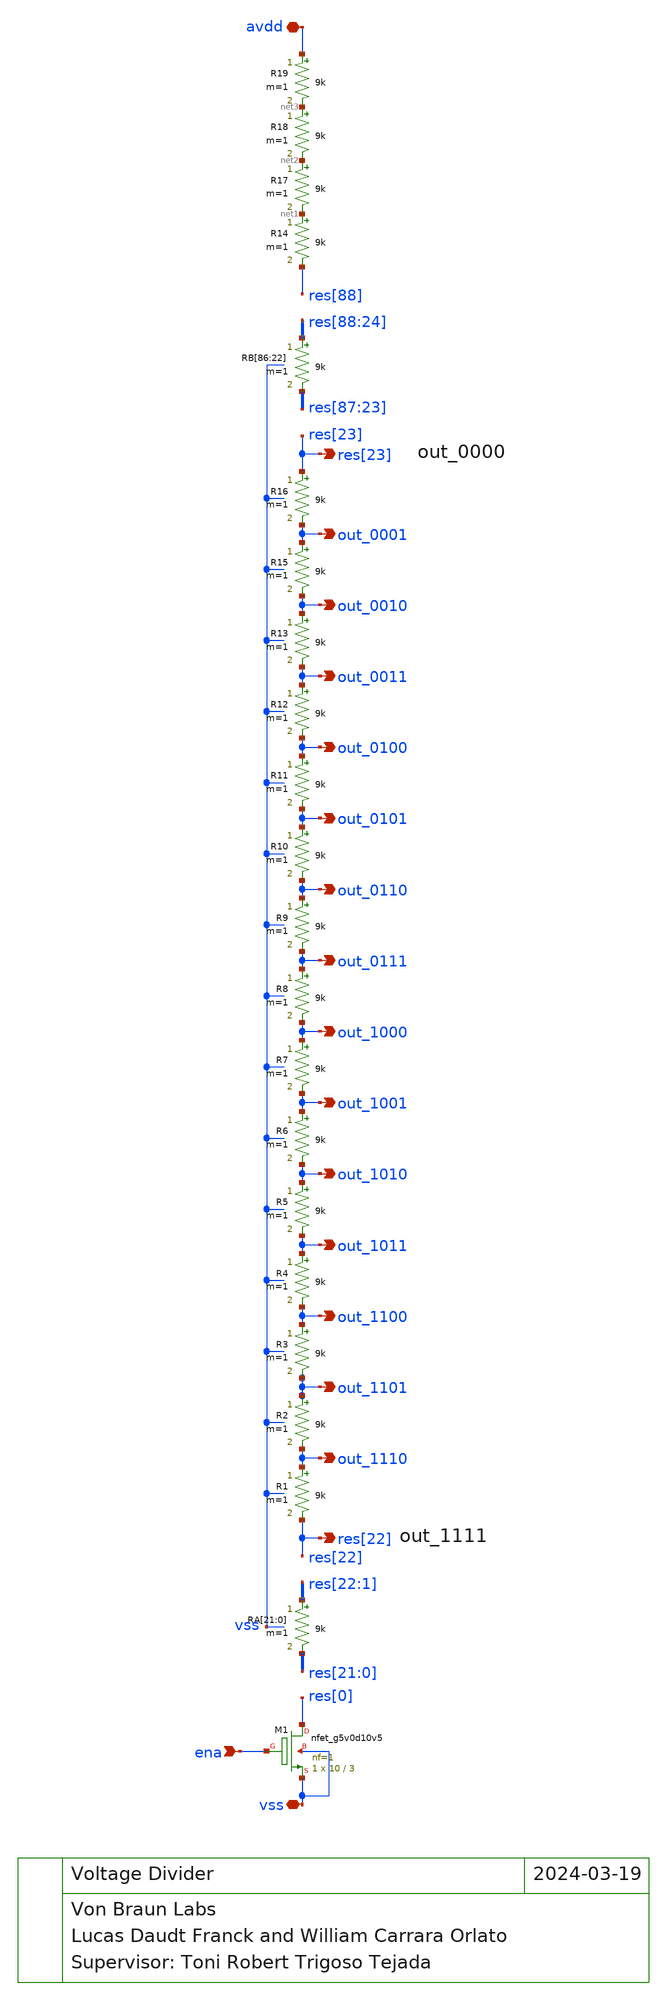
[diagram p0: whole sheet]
** sch_path: blocks/input/xschem/divisor_completo.sch
**.subckt divisor_completo ena vss avdd res[22] out_1110 out_1101 out_1100 out_1011 out_1010
*+ out_1001 out_1000 out_0111 out_0110 out_0101 out_0100 out_0011 out_0010 out_0001 res[23]
*.ipin ena
*.iopin vss
*.iopin avdd
*.opin res[22]
*.opin out_1110
*.opin out_1101
*.opin out_1100
*.opin out_1011
*.opin out_1010
*.opin out_1001
*.opin out_1000
*.opin out_0111
*.opin out_0110
*.opin out_0101
*.opin out_0100
*.opin out_0011
*.opin out_0010
*.opin out_0001
*.opin res[23]
XM1 res[0] ena vss vss sky130_fd_pr__nfet_g5v0d10v5 L=3 W=10 nf=1 ad='int((nf+1)/2) * W/nf * 0.29' as='int((nf+2)/2) * W/nf * 0.29'
+ pd='2*int((nf+1)/2) * (W/nf + 0.29)' ps='2*int((nf+2)/2) * (W/nf + 0.29)' nrd='0.29 / W' nrs='0.29 / W'
+ sa=0 sb=0 sd=0 mult=1 m=1
RA[21] res[22] res[21] 9k m=1
RA[20] res[21] res[20] 9k m=1
RA[19] res[20] res[19] 9k m=1
RA[18] res[19] res[18] 9k m=1
RA[17] res[18] res[17] 9k m=1
RA[16] res[17] res[16] 9k m=1
RA[15] res[16] res[15] 9k m=1
RA[14] res[15] res[14] 9k m=1
RA[13] res[14] res[13] 9k m=1
RA[12] res[13] res[12] 9k m=1
RA[11] res[12] res[11] 9k m=1
RA[10] res[11] res[10] 9k m=1
RA[9] res[10] res[9] 9k m=1
RA[8] res[9] res[8] 9k m=1
RA[7] res[8] res[7] 9k m=1
RA[6] res[7] res[6] 9k m=1
RA[5] res[6] res[5] 9k m=1
RA[4] res[5] res[4] 9k m=1
RA[3] res[4] res[3] 9k m=1
RA[2] res[3] res[2] 9k m=1
RA[1] res[2] res[1] 9k m=1
RA[0] res[1] res[0] 9k m=1
R2 out_1101 out_1110 9k m=1
R1 out_1110 res[22] 9k m=1
R3 out_1100 out_1101 9k m=1
R4 out_1011 out_1100 9k m=1
R5 out_1010 out_1011 9k m=1
R6 out_1001 out_1010 9k m=1
R7 out_1000 out_1001 9k m=1
R8 out_0111 out_1000 9k m=1
R9 out_0110 out_0111 9k m=1
R10 out_0101 out_0110 9k m=1
R11 out_0100 out_0101 9k m=1
R12 out_0011 out_0100 9k m=1
R13 out_0010 out_0011 9k m=1
R15 out_0001 out_0010 9k m=1
R16 res[23] out_0001 9k m=1
RB[86] res[88] res[87] 9k m=1
RB[85] res[87] res[86] 9k m=1
RB[84] res[86] res[85] 9k m=1
RB[83] res[85] res[84] 9k m=1
RB[82] res[84] res[83] 9k m=1
RB[81] res[83] res[82] 9k m=1
RB[80] res[82] res[81] 9k m=1
RB[79] res[81] res[80] 9k m=1
RB[78] res[80] res[79] 9k m=1
RB[77] res[79] res[78] 9k m=1
RB[76] res[78] res[77] 9k m=1
RB[75] res[77] res[76] 9k m=1
RB[74] res[76] res[75] 9k m=1
RB[73] res[75] res[74] 9k m=1
RB[72] res[74] res[73] 9k m=1
RB[71] res[73] res[72] 9k m=1
RB[70] res[72] res[71] 9k m=1
RB[69] res[71] res[70] 9k m=1
RB[68] res[70] res[69] 9k m=1
RB[67] res[69] res[68] 9k m=1
RB[66] res[68] res[67] 9k m=1
RB[65] res[67] res[66] 9k m=1
RB[64] res[66] res[65] 9k m=1
RB[63] res[65] res[64] 9k m=1
RB[62] res[64] res[63] 9k m=1
RB[61] res[63] res[62] 9k m=1
RB[60] res[62] res[61] 9k m=1
RB[59] res[61] res[60] 9k m=1
RB[58] res[60] res[59] 9k m=1
RB[57] res[59] res[58] 9k m=1
RB[56] res[58] res[57] 9k m=1
RB[55] res[57] res[56] 9k m=1
RB[54] res[56] res[55] 9k m=1
RB[53] res[55] res[54] 9k m=1
RB[52] res[54] res[53] 9k m=1
RB[51] res[53] res[52] 9k m=1
RB[50] res[52] res[51] 9k m=1
RB[49] res[51] res[50] 9k m=1
RB[48] res[50] res[49] 9k m=1
RB[47] res[49] res[48] 9k m=1
RB[46] res[48] res[47] 9k m=1
RB[45] res[47] res[46] 9k m=1
RB[44] res[46] res[45] 9k m=1
RB[43] res[45] res[44] 9k m=1
RB[42] res[44] res[43] 9k m=1
RB[41] res[43] res[42] 9k m=1
RB[40] res[42] res[41] 9k m=1
RB[39] res[41] res[40] 9k m=1
RB[38] res[40] res[39] 9k m=1
RB[37] res[39] res[38] 9k m=1
RB[36] res[38] res[37] 9k m=1
RB[35] res[37] res[36] 9k m=1
RB[34] res[36] res[35] 9k m=1
RB[33] res[35] res[34] 9k m=1
RB[32] res[34] res[33] 9k m=1
RB[31] res[33] res[32] 9k m=1
RB[30] res[32] res[31] 9k m=1
RB[29] res[31] res[30] 9k m=1
RB[28] res[30] res[29] 9k m=1
RB[27] res[29] res[28] 9k m=1
RB[26] res[28] res[27] 9k m=1
RB[25] res[27] res[26] 9k m=1
RB[24] res[26] res[25] 9k m=1
RB[23] res[25] res[24] 9k m=1
RB[22] res[24] res[23] 9k m=1
R14 net1 res[88] 9k m=1
R17 net2 net1 9k m=1
R18 net3 net2 9k m=1
R19 avdd net3 9k m=1
**.ends
.end
